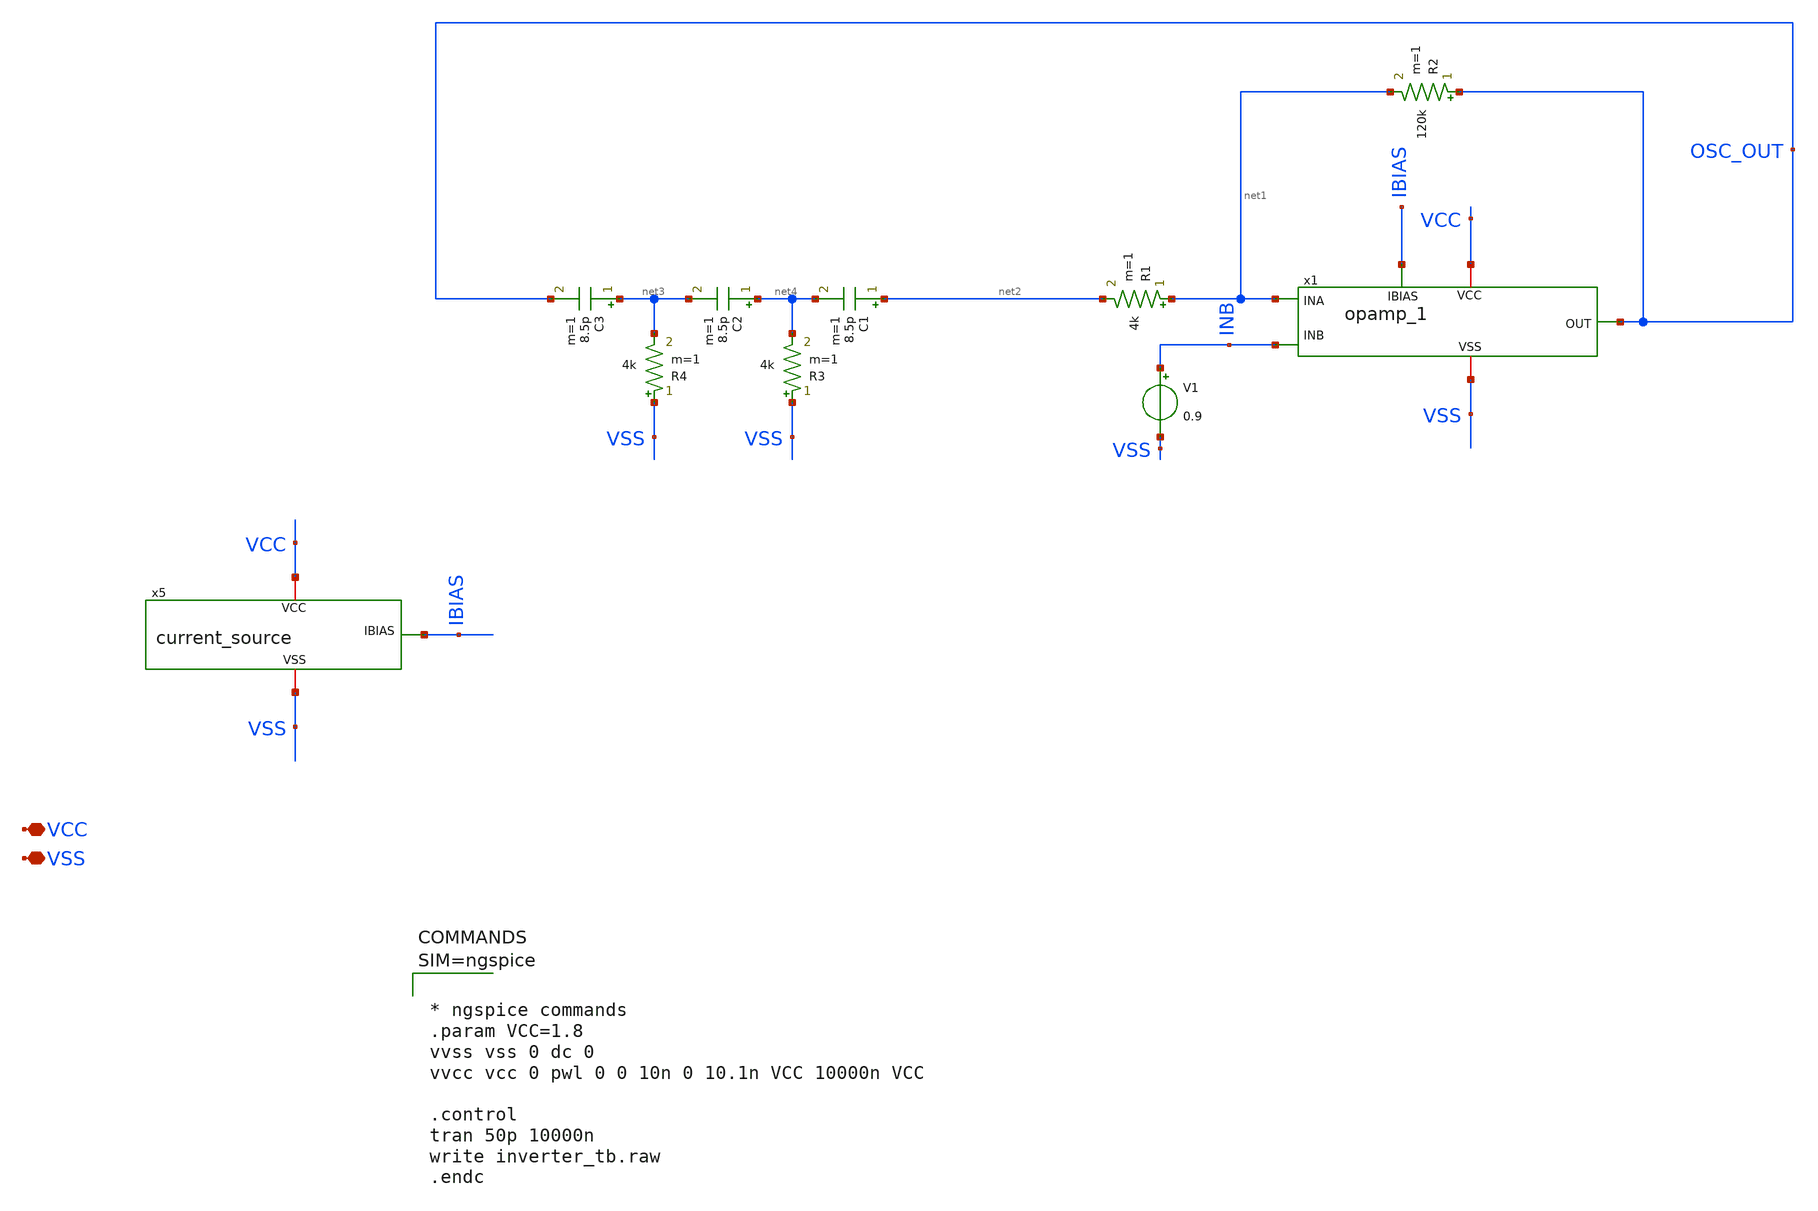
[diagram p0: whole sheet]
** sch_path: xschem/ps_oscillator_20mhz.sch
**.subckt ps_oscillator_20mhz VCC VSS
*.iopin VCC
*.iopin VSS
x1 VCC OSC_OUT net1 INB VSS IBIAS opamp_1
x5 VCC VSS IBIAS current_source
V1 INB VSS 0.9
R1 net1 net2 4k m=1
R2 OSC_OUT net1 120k m=1
C1 net2 net4 8.5p m=1
C2 net4 net3 8.5p m=1
C3 net3 OSC_OUT 8.5p m=1
R3 VSS net4 4k m=1
R4 VSS net3 4k m=1
**** begin user architecture code

** opencircuitdesign pdks install
.lib $::SKYWATER_MODELS/sky130.lib.spice tt





* ngspice commands
.param VCC=1.8
vvss vss 0 dc 0
vvcc vcc 0 pwl 0 0 10n 0 10.1n VCC 10000n VCC

.control
tran 50p 10000n
write inverter_tb.raw
.endc




**** end user architecture code
**.ends

* expanding   symbol:  opamp_1.sym # of pins=6
** sym_path: xschem/opamp_1.sym
** sch_path: xschem/opamp_1.sch
.subckt opamp_1 VCC OUT INA INB VSS IBIAS
*.ipin INA
*.ipin INB
*.opin OUT
*.iopin VCC
*.iopin VSS
*.ipin IBIAS
XM1 MIRR INA TAILV VSS sky130_fd_pr__nfet_01v8 L=1 W=20 nf=1 ad='int((nf+1)/2) * W/nf * 0.29' as='int((nf+2)/2) * W/nf * 0.29'
+ pd='2*int((nf+1)/2) * (W/nf + 0.29)' ps='2*int((nf+2)/2) * (W/nf + 0.29)' nrd='0.29 / W' nrs='0.29 / W'
+ sa=0 sb=0 sd=0 mult=1 m=1
XM2 DIFF_OUT INB TAILV VSS sky130_fd_pr__nfet_01v8 L=1 W=20 nf=1 ad='int((nf+1)/2) * W/nf * 0.29' as='int((nf+2)/2) * W/nf * 0.29'
+ pd='2*int((nf+1)/2) * (W/nf + 0.29)' ps='2*int((nf+2)/2) * (W/nf + 0.29)' nrd='0.29 / W' nrs='0.29 / W'
+ sa=0 sb=0 sd=0 mult=1 m=1
XM3 TAILV IBIAS VSS VSS sky130_fd_pr__nfet_01v8 L=1 W=40 nf=1 ad='int((nf+1)/2) * W/nf * 0.29' as='int((nf+2)/2) * W/nf * 0.29'
+ pd='2*int((nf+1)/2) * (W/nf + 0.29)' ps='2*int((nf+2)/2) * (W/nf + 0.29)' nrd='0.29 / W' nrs='0.29 / W'
+ sa=0 sb=0 sd=0 mult=1 m=1
XM4 MIRR MIRR VCC VCC sky130_fd_pr__pfet_01v8_lvt L=0.5 W=14 nf=1 ad='int((nf+1)/2) * W/nf * 0.29' as='int((nf+2)/2) * W/nf * 0.29'
+ pd='2*int((nf+1)/2) * (W/nf + 0.29)' ps='2*int((nf+2)/2) * (W/nf + 0.29)' nrd='0.29 / W' nrs='0.29 / W'
+ sa=0 sb=0 sd=0 mult=1 m=1
XM5 DIFF_OUT MIRR VCC VCC sky130_fd_pr__pfet_01v8_lvt L=0.5 W=14 nf=1 ad='int((nf+1)/2) * W/nf * 0.29'
+ as='int((nf+2)/2) * W/nf * 0.29' pd='2*int((nf+1)/2) * (W/nf + 0.29)' ps='2*int((nf+2)/2) * (W/nf + 0.29)'
+ nrd='0.29 / W' nrs='0.29 / W' sa=0 sb=0 sd=0 mult=1 m=1
XM6 OUT IBIAS VSS VSS sky130_fd_pr__nfet_01v8 L=0.5 W=93 nf=1 ad='int((nf+1)/2) * W/nf * 0.29' as='int((nf+2)/2) * W/nf * 0.29'
+ pd='2*int((nf+1)/2) * (W/nf + 0.29)' ps='2*int((nf+2)/2) * (W/nf + 0.29)' nrd='0.29 / W' nrs='0.29 / W'
+ sa=0 sb=0 sd=0 mult=1 m=1
XM7 OUT DIFF_OUT VCC VCC sky130_fd_pr__pfet_01v8_lvt L=0.5 W=70 nf=1 ad='int((nf+1)/2) * W/nf * 0.29'
+ as='int((nf+2)/2) * W/nf * 0.29' pd='2*int((nf+1)/2) * (W/nf + 0.29)' ps='2*int((nf+2)/2) * (W/nf + 0.29)'
+ nrd='0.29 / W' nrs='0.29 / W' sa=0 sb=0 sd=0 mult=1 m=1
XM9 RBIAS IBIAS VSS VSS sky130_fd_pr__nfet_01v8 L=1 W=5 nf=1 ad='int((nf+1)/2) * W/nf * 0.29' as='int((nf+2)/2) * W/nf * 0.29'
+ pd='2*int((nf+1)/2) * (W/nf + 0.29)' ps='2*int((nf+2)/2) * (W/nf + 0.29)' nrd='0.29 / W' nrs='0.29 / W'
+ sa=0 sb=0 sd=0 mult=1 m=1
XM10 RBIAS RBIAS net2 VCC sky130_fd_pr__pfet_01v8_lvt L=0.5 W=1 nf=1 ad='int((nf+1)/2) * W/nf * 0.29'
+ as='int((nf+2)/2) * W/nf * 0.29' pd='2*int((nf+1)/2) * (W/nf + 0.29)' ps='2*int((nf+2)/2) * (W/nf + 0.29)'
+ nrd='0.29 / W' nrs='0.29 / W' sa=0 sb=0 sd=0 mult=1 m=1
XM11 net2 net2 VCC VCC sky130_fd_pr__pfet_01v8_lvt L=0.5 W=7.5 nf=1 ad='int((nf+1)/2) * W/nf * 0.29'
+ as='int((nf+2)/2) * W/nf * 0.29' pd='2*int((nf+1)/2) * (W/nf + 0.29)' ps='2*int((nf+2)/2) * (W/nf + 0.29)'
+ nrd='0.29 / W' nrs='0.29 / W' sa=0 sb=0 sd=0 mult=1 m=1
XC1 OUT net1 sky130_fd_pr__cap_mim_m3_2 W=20 L=13 MF=1 m=1
XM8 net1 RBIAS DIFF_OUT VCC sky130_fd_pr__pfet_01v8_lvt L=0.5 W=14 nf=1 ad='int((nf+1)/2) * W/nf * 0.29'
+ as='int((nf+2)/2) * W/nf * 0.29' pd='2*int((nf+1)/2) * (W/nf + 0.29)' ps='2*int((nf+2)/2) * (W/nf + 0.29)'
+ nrd='0.29 / W' nrs='0.29 / W' sa=0 sb=0 sd=0 mult=1 m=1
.ends


* expanding   symbol:  current_source.sym # of pins=3
** sym_path: xschem/current_source.sym
** sch_path: xschem/current_source.sch
.subckt current_source VCC VSS IBIAS
*.iopin VCC
*.iopin VSS
*.opin IBIAS
XM3 IBIAS IBIAS VSS VSS sky130_fd_pr__nfet_01v8 L=1 W=40 nf=1 ad='int((nf+1)/2) * W/nf * 0.29' as='int((nf+2)/2) * W/nf * 0.29'
+ pd='2*int((nf+1)/2) * (W/nf + 0.29)' ps='2*int((nf+2)/2) * (W/nf + 0.29)' nrd='0.29 / W' nrs='0.29 / W'
+ sa=0 sb=0 sd=0 mult=1 m=1
XR1 IBIAS VCC sky130_fd_pr__res_generic_po W=0.33 L=12 m=1
.ends

.end
